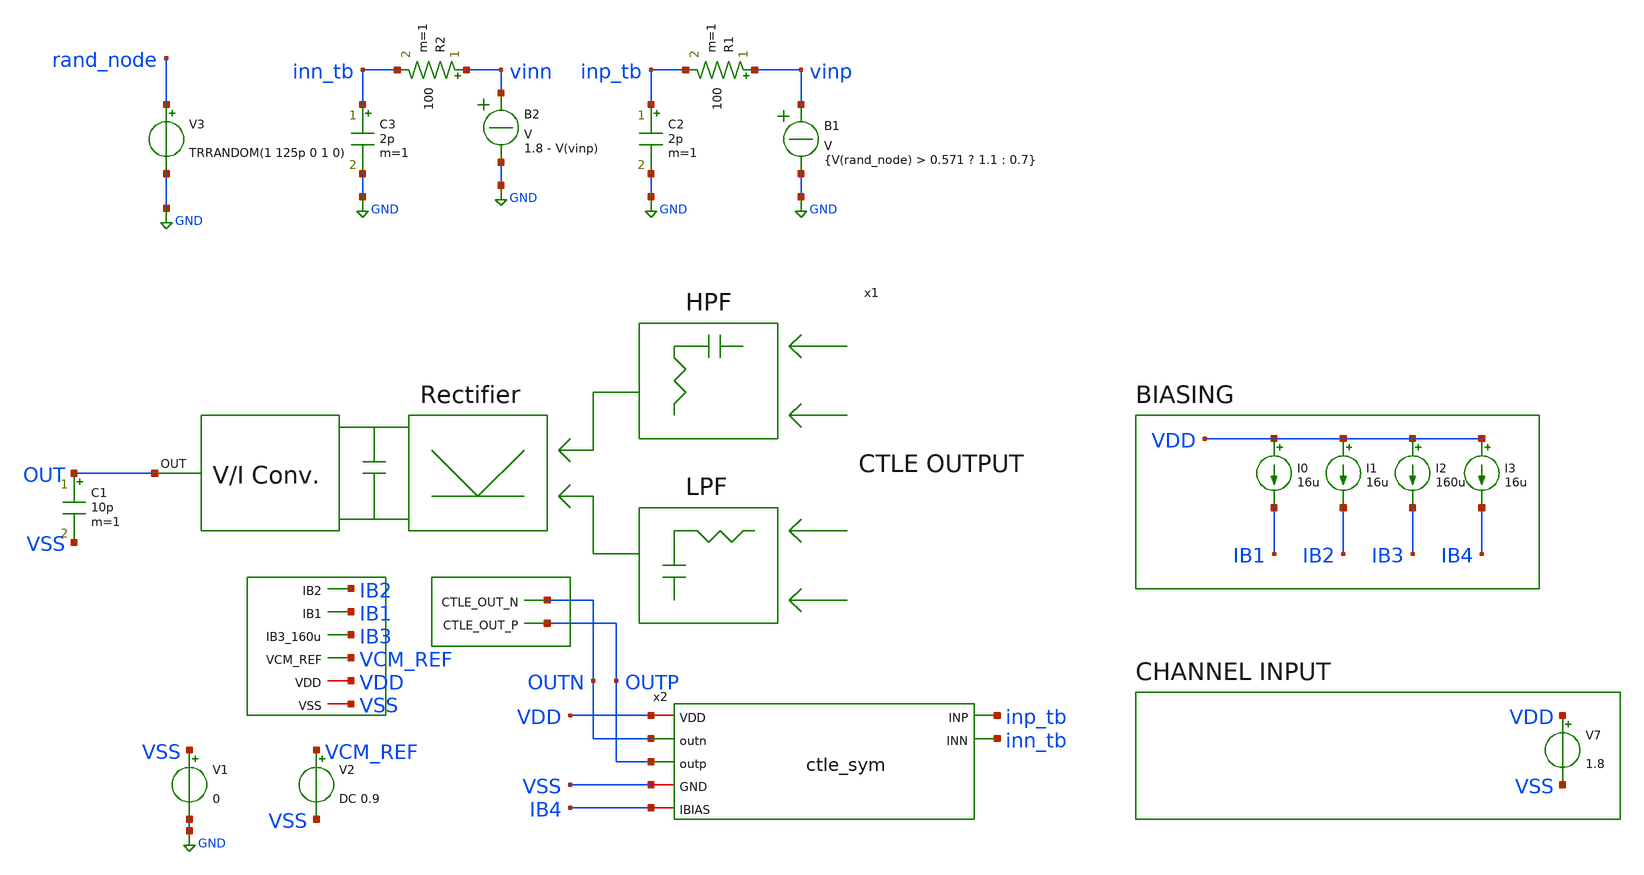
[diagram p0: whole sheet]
** sch_path: pd-converter/tb_adaptation-loop-baseline.sch
**.subckt tb_adaptation-loop-baseline
x1 IB2 VDD OUT IB1 VSS VCM_REF IB3 OUTN OUTP vctrl-generator
x2 VDD OUTN OUTP inp_tb inn_tb VSS IB4 ctle_sym
I0 VDD IB1 16u
I1 VDD IB2 16u
I2 VDD IB3 160u
V7 VDD VSS 1.8
I3 VDD IB4 16u
V1 VSS GND 0
V2 VCM_REF VSS DC 0.9
C1 OUT VSS 10p m=1
R1 vinp inp_tb 100 m=1
C2 inp_tb GND 2p m=1
V3 rand_node GND TRRANDOM(1 125p 0 1 0)
R2 vinn inn_tb 100 m=1
C3 inn_tb GND 2p m=1
B1 vinp GND V = {V(rand_node) > 0.571 ? 1.1 : 0.7}
B2 vinn GND V = 1.8 - V(vinp)
**** begin user architecture code

.lib /foss/pdks/sky130A/libs.tech/ngspice/sky130.lib.spice tt

.control
  tran 1p 500n

  * --- Eye diagram (same as tb_eye) ---
  let period = 250e-12
  let t_mod = time - floor(time / period) * period
  plot v(outp) vs t_mod title Eye - outp
  plot v(outp) v(outn) vs t_mod title Differential Eye

  * --- Adaptation convergence ---
  plot v(OUT) title IBIAS adaptation convergence

  * --- Compare: adaptation vs fixed bias eye quality ---
  * Run twice: once with Xadapt, once with ibias_adapt=ibias_ref fixed
  * and visually compare eye opening

  * --- Measurements ---
  meas tran vout_max  MAX  v(outp)  FROM=50n  TO=100n
  meas tran vout_min  MIN  v(outp)  FROM=50n  TO=100n
  let eye_height_single = vout_max - vout_min
  print eye_height_single

  meas tran ibias_final  AVG  v(OUT)  FROM=80n  TO=100n
  print ibias_final

.endc


**** end user architecture code
**.ends

* expanding   symbol:  vctrl-generator.sym # of pins=9
** sym_path: pd-converter/vctrl-generator.sym
** sch_path: pd-converter/vctrl-generator.sch
.subckt vctrl-generator IB2 VDD OUT IB1 VSS VCM_REF IB3_160u CTLE_OUT_N CTLE_OUT_P
*.ipin IB1
*.ipin IB2
*.ipin IB3_160u
*.iopin VDD
*.iopin VSS
*.opin OUT
*.ipin CTLE_OUT_N
*.ipin CTLE_OUT_P
*.ipin VCM_REF
x1 VDD net1 net2 IB3_160u VSS VCM_REF CTLE_OUT_N CTLE_OUT_P filterred_power_detector_sizing
x2 VDD IB2 IB1 OUT net2 net1 VCM_REF VSS voltage-to-i-converter
.ends


* expanding   symbol:  /foss/designs/afe-icdec-teknofest-2026/CTLE/ctle_sym.sym # of pins=7
** sym_path: CTLE/ctle_sym.sym
** sch_path: CTLE/ctle_sym.sch
.subckt ctle_sym VDD outn outp INP INN GND IBIAS
*.opin outp
*.opin outn
*.ipin INN
*.iopin VDD
*.iopin GND
*.iopin IBIAS
*.ipin INP
XM1 outp INP net1 GND sky130_fd_pr__nfet_01v8_lvt L=0.15 W=2 nf=1 ad='int((nf+1)/2) * W/nf * 0.29' as='int((nf+2)/2) * W/nf * 0.29'
+ pd='2*int((nf+1)/2) * (W/nf + 0.29)' ps='2*int((nf+2)/2) * (W/nf + 0.29)' nrd='0.29 / W' nrs='0.29 / W'
+ sa=0 sb=0 sd=0 mult=15 m=15
XM2 outn INN net2 GND sky130_fd_pr__nfet_01v8_lvt L=0.15 W=2 nf=1 ad='int((nf+1)/2) * W/nf * 0.29' as='int((nf+2)/2) * W/nf * 0.29'
+ pd='2*int((nf+1)/2) * (W/nf + 0.29)' ps='2*int((nf+2)/2) * (W/nf + 0.29)' nrd='0.29 / W' nrs='0.29 / W'
+ sa=0 sb=0 sd=0 mult=15 m=15
XM3 net1 IBIAS GND GND sky130_fd_pr__nfet_01v8_lvt L=1 W=2 nf=1 ad='int((nf+1)/2) * W/nf * 0.29' as='int((nf+2)/2) * W/nf * 0.29'
+ pd='2*int((nf+1)/2) * (W/nf + 0.29)' ps='2*int((nf+2)/2) * (W/nf + 0.29)' nrd='0.29 / W' nrs='0.29 / W'
+ sa=0 sb=0 sd=0 mult=24 m=24
XM4 net2 IBIAS GND GND sky130_fd_pr__nfet_01v8_lvt L=1 W=2 nf=1 ad='int((nf+1)/2) * W/nf * 0.29' as='int((nf+2)/2) * W/nf * 0.29'
+ pd='2*int((nf+1)/2) * (W/nf + 0.29)' ps='2*int((nf+2)/2) * (W/nf + 0.29)' nrd='0.29 / W' nrs='0.29 / W'
+ sa=0 sb=0 sd=0 mult=24 m=24
XM5 IBIAS IBIAS GND GND sky130_fd_pr__nfet_01v8_lvt L=1 W=2 nf=1 ad='int((nf+1)/2) * W/nf * 0.29' as='int((nf+2)/2) * W/nf * 0.29'
+ pd='2*int((nf+1)/2) * (W/nf + 0.29)' ps='2*int((nf+2)/2) * (W/nf + 0.29)' nrd='0.29 / W' nrs='0.29 / W'
+ sa=0 sb=0 sd=0 mult=1 m=1
RD1 VDD outp 280 m=1
RD2 VDD outn 280 m=1
CS net1 net2 134f m=1
RS net1 net2 1400 m=1
C1 outp GND 20f m=1
C2 outn GND 20f m=1
.ends


* expanding   symbol:
*+  /foss/designs/afe-icdec-teknofest-2026/CTLE/filterred_power_detector_sizing.sym # of pins=8
** sym_path: CTLE/filterred_power_detector_sizing.sym
** sch_path: CTLE/filterred_power_detector_sizing.sch
.subckt filterred_power_detector_sizing vdd voutp voutn ibias vss vcmref vinn vinp
*.ipin vinp
*.ipin vinn
*.opin voutp
*.opin voutn
*.ipin ibias
*.iopin vss
*.iopin vdd
*.ipin vcmref
XM1 voutp Vhf_pos net1 vss sky130_fd_pr__nfet_01v8 L=0.45 W=1.23 nf=1 ad='int((nf+1)/2) * W/nf * 0.29'
+ as='int((nf+2)/2) * W/nf * 0.29' pd='2*int((nf+1)/2) * (W/nf + 0.29)' ps='2*int((nf+2)/2) * (W/nf + 0.29)'
+ nrd='0.29 / W' nrs='0.29 / W' sa=0 sb=0 sd=0 mult=1 m=1
XM2 voutp Vhf_neg net1 vss sky130_fd_pr__nfet_01v8 L=0.45 W=1.23 nf=1 ad='int((nf+1)/2) * W/nf * 0.29'
+ as='int((nf+2)/2) * W/nf * 0.29' pd='2*int((nf+1)/2) * (W/nf + 0.29)' ps='2*int((nf+2)/2) * (W/nf + 0.29)'
+ nrd='0.29 / W' nrs='0.29 / W' sa=0 sb=0 sd=0 mult=1 m=1
XM3 voutn Vlf_pos net1 vss sky130_fd_pr__nfet_01v8 L=0.75 W=1.23 nf=1 ad='int((nf+1)/2) * W/nf * 0.29'
+ as='int((nf+2)/2) * W/nf * 0.29' pd='2*int((nf+1)/2) * (W/nf + 0.29)' ps='2*int((nf+2)/2) * (W/nf + 0.29)'
+ nrd='0.29 / W' nrs='0.29 / W' sa=0 sb=0 sd=0 mult=1 m=1
XM4 voutn Vlf_neg net1 vss sky130_fd_pr__nfet_01v8 L=0.45 W=1.23 nf=1 ad='int((nf+1)/2) * W/nf * 0.29'
+ as='int((nf+2)/2) * W/nf * 0.29' pd='2*int((nf+1)/2) * (W/nf + 0.29)' ps='2*int((nf+2)/2) * (W/nf + 0.29)'
+ nrd='0.29 / W' nrs='0.29 / W' sa=0 sb=0 sd=0 mult=1 m=1
XC7 Vhf_neg vinn sky130_fd_pr__cap_mim_m3_1 W=5.7921 L=5.7921 MF=1 m=1
XC3 Vhf_pos vinp sky130_fd_pr__cap_mim_m3_1 W=5.7921 L=5.7921 MF=1 m=1
XR9 Vhf_neg net2 vss sky130_fd_pr__res_high_po_5p73 L=69.65 mult=4 m=4
XR3 net2 Vhf_pos vss sky130_fd_pr__res_high_po_5p73 L=69.65 mult=4 m=4
XR4 vcmref vinn vss sky130_fd_pr__res_high_po_5p73 L=708 mult=4 m=4
XR5 vinp vcmref vss sky130_fd_pr__res_high_po_5p73 L=708 mult=4 m=4
XC4 net2 vss sky130_fd_pr__cap_mim_m3_1 W=0.4208 L=0.4208 MF=1 m=1
XR6 Vlf_pos vinp vss sky130_fd_pr__res_high_po_5p73 L=69.65 mult=4 m=4
XR7 vinn Vlf_neg vss sky130_fd_pr__res_high_po_5p73 L=69.65 mult=4 m=4
XC2 Vlf_pos vss sky130_fd_pr__cap_mim_m3_1 W=5.7921 L=5.7921 MF=1 m=1
XC5 vss Vlf_neg sky130_fd_pr__cap_mim_m3_1 W=5.7921 L=5.7921 MF=1 m=1
XC6 voutp voutn sky130_fd_pr__cap_mim_m3_1 W=0.2019 L=0.2019 MF=1 m=1
XR8 voutp vdd vss sky130_fd_pr__res_high_po_5p73 L=796.338 mult=4 m=4
XR1 voutn vdd vss sky130_fd_pr__res_high_po_5p73 L=796.338 mult=4 m=4
XM5 net1 ibias vss vss sky130_fd_pr__nfet_01v8 L=0.45 W=4.92 nf=1 ad='int((nf+1)/2) * W/nf * 0.29' as='int((nf+2)/2) * W/nf * 0.29'
+ pd='2*int((nf+1)/2) * (W/nf + 0.29)' ps='2*int((nf+2)/2) * (W/nf + 0.29)' nrd='0.29 / W' nrs='0.29 / W'
+ sa=0 sb=0 sd=0 mult=1 m=1
XM6 ibias ibias vss vss sky130_fd_pr__nfet_01v8 L=0.45 W=0.45 nf=1 ad='int((nf+1)/2) * W/nf * 0.29' as='int((nf+2)/2) * W/nf * 0.29'
+ pd='2*int((nf+1)/2) * (W/nf + 0.29)' ps='2*int((nf+2)/2) * (W/nf + 0.29)' nrd='0.29 / W' nrs='0.29 / W'
+ sa=0 sb=0 sd=0 mult=1 m=1
.ends


* expanding   symbol:  /foss/designs/afe-icdec-teknofest-2026/CTLE/voltage-to-i-converter.sym # of
*+ pins=8
** sym_path: CTLE/voltage-to-i-converter.sym
** sch_path: CTLE/voltage-to-i-converter.sch
.subckt voltage-to-i-converter VDD IB2_16u IB1_16u OUT DOWN UP vcmref VSS
*.iopin VDD
*.iopin VSS
*.opin OUT
*.ipin IB2_16u
*.ipin UP
*.ipin DOWN
*.ipin IB1_16u
*.ipin vcmref
XM1 net3 net3 VDD VDD sky130_fd_pr__pfet_01v8 L=0.6 W=75 nf=1 ad='int((nf+1)/2) * W/nf * 0.29' as='int((nf+2)/2) * W/nf * 0.29'
+ pd='2*int((nf+1)/2) * (W/nf + 0.29)' ps='2*int((nf+2)/2) * (W/nf + 0.29)' nrd='0.29 / W' nrs='0.29 / W'
+ sa=0 sb=0 sd=0 mult=1 m=1
XM2 net5 net5 VDD VDD sky130_fd_pr__pfet_01v8 L=0.6 W=75 nf=1 ad='int((nf+1)/2) * W/nf * 0.29' as='int((nf+2)/2) * W/nf * 0.29'
+ pd='2*int((nf+1)/2) * (W/nf + 0.29)' ps='2*int((nf+2)/2) * (W/nf + 0.29)' nrd='0.29 / W' nrs='0.29 / W'
+ sa=0 sb=0 sd=0 mult=1 m=1
XM5 net1 IB1_16u VSS VSS sky130_fd_pr__nfet_01v8 L=1.5 W=25 nf=1 ad='int((nf+1)/2) * W/nf * 0.29' as='int((nf+2)/2) * W/nf * 0.29'
+ pd='2*int((nf+1)/2) * (W/nf + 0.29)' ps='2*int((nf+2)/2) * (W/nf + 0.29)' nrd='0.29 / W' nrs='0.29 / W'
+ sa=0 sb=0 sd=0 mult=1 m=1
XM6 IB1_16u IB1_16u VSS VSS sky130_fd_pr__nfet_01v8 L=1.5 W=25 nf=1 ad='int((nf+1)/2) * W/nf * 0.29'
+ as='int((nf+2)/2) * W/nf * 0.29' pd='2*int((nf+1)/2) * (W/nf + 0.29)' ps='2*int((nf+2)/2) * (W/nf + 0.29)'
+ nrd='0.29 / W' nrs='0.29 / W' sa=0 sb=0 sd=0 mult=1 m=1
XM7 net4 net4 VDD VDD sky130_fd_pr__pfet_01v8 L=0.6 W=75 nf=1 ad='int((nf+1)/2) * W/nf * 0.29' as='int((nf+2)/2) * W/nf * 0.29'
+ pd='2*int((nf+1)/2) * (W/nf + 0.29)' ps='2*int((nf+2)/2) * (W/nf + 0.29)' nrd='0.29 / W' nrs='0.29 / W'
+ sa=0 sb=0 sd=0 mult=1 m=1
XM8 net6 net6 VDD VDD sky130_fd_pr__pfet_01v8 L=0.6 W=75 nf=1 ad='int((nf+1)/2) * W/nf * 0.29' as='int((nf+2)/2) * W/nf * 0.29'
+ pd='2*int((nf+1)/2) * (W/nf + 0.29)' ps='2*int((nf+2)/2) * (W/nf + 0.29)' nrd='0.29 / W' nrs='0.29 / W'
+ sa=0 sb=0 sd=0 mult=1 m=1
XM11 net2 IB2_16u VSS VSS sky130_fd_pr__nfet_01v8 L=1.5 W=25 nf=1 ad='int((nf+1)/2) * W/nf * 0.29' as='int((nf+2)/2) * W/nf * 0.29'
+ pd='2*int((nf+1)/2) * (W/nf + 0.29)' ps='2*int((nf+2)/2) * (W/nf + 0.29)' nrd='0.29 / W' nrs='0.29 / W'
+ sa=0 sb=0 sd=0 mult=1 m=1
XM12 IB2_16u IB2_16u VSS VSS sky130_fd_pr__nfet_01v8 L=1.5 W=25 nf=1 ad='int((nf+1)/2) * W/nf * 0.29'
+ as='int((nf+2)/2) * W/nf * 0.29' pd='2*int((nf+1)/2) * (W/nf + 0.29)' ps='2*int((nf+2)/2) * (W/nf + 0.29)'
+ nrd='0.29 / W' nrs='0.29 / W' sa=0 sb=0 sd=0 mult=1 m=1
XM13 OUT net6 VDD VDD sky130_fd_pr__pfet_01v8 L=0.6 W=75 nf=1 ad='int((nf+1)/2) * W/nf * 0.29' as='int((nf+2)/2) * W/nf * 0.29'
+ pd='2*int((nf+1)/2) * (W/nf + 0.29)' ps='2*int((nf+2)/2) * (W/nf + 0.29)' nrd='0.29 / W' nrs='0.29 / W'
+ sa=0 sb=0 sd=0 mult=1 m=1
XM14 net7 net5 VDD VDD sky130_fd_pr__pfet_01v8 L=0.6 W=75 nf=1 ad='int((nf+1)/2) * W/nf * 0.29' as='int((nf+2)/2) * W/nf * 0.29'
+ pd='2*int((nf+1)/2) * (W/nf + 0.29)' ps='2*int((nf+2)/2) * (W/nf + 0.29)' nrd='0.29 / W' nrs='0.29 / W'
+ sa=0 sb=0 sd=0 mult=1 m=1
XM15 net7 net7 VSS VSS sky130_fd_pr__nfet_01v8 L=1.5 W=25 nf=1 ad='int((nf+1)/2) * W/nf * 0.29' as='int((nf+2)/2) * W/nf * 0.29'
+ pd='2*int((nf+1)/2) * (W/nf + 0.29)' ps='2*int((nf+2)/2) * (W/nf + 0.29)' nrd='0.29 / W' nrs='0.29 / W'
+ sa=0 sb=0 sd=0 mult=1 m=1
XM16 OUT net7 VSS VSS sky130_fd_pr__nfet_01v8 L=1.5 W=25 nf=1 ad='int((nf+1)/2) * W/nf * 0.29' as='int((nf+2)/2) * W/nf * 0.29'
+ pd='2*int((nf+1)/2) * (W/nf + 0.29)' ps='2*int((nf+2)/2) * (W/nf + 0.29)' nrd='0.29 / W' nrs='0.29 / W'
+ sa=0 sb=0 sd=0 mult=1 m=1
XR1 DOWN vcmref VSS sky130_fd_pr__res_high_po_0p35 L=50 mult=1 m=1
XR2 vcmref UP VSS sky130_fd_pr__res_high_po_0p35 L=50 mult=1 m=1
XC1 OUT VSS sky130_fd_pr__cap_mim_m3_1 W=30 L=30 MF=4 m=4
XM3 net5 DOWN net1 VSS sky130_fd_pr__nfet_01v8 L=0.5 W=25 nf=1 ad='int((nf+1)/2) * W/nf * 0.29' as='int((nf+2)/2) * W/nf * 0.29'
+ pd='2*int((nf+1)/2) * (W/nf + 0.29)' ps='2*int((nf+2)/2) * (W/nf + 0.29)' nrd='0.29 / W' nrs='0.29 / W'
+ sa=0 sb=0 sd=0 mult=1 m=1
XM4 net3 vcmref net1 VSS sky130_fd_pr__nfet_01v8 L=0.5 W=25 nf=1 ad='int((nf+1)/2) * W/nf * 0.29' as='int((nf+2)/2) * W/nf * 0.29'
+ pd='2*int((nf+1)/2) * (W/nf + 0.29)' ps='2*int((nf+2)/2) * (W/nf + 0.29)' nrd='0.29 / W' nrs='0.29 / W'
+ sa=0 sb=0 sd=0 mult=1 m=1
XM9 net4 vcmref net2 VSS sky130_fd_pr__nfet_01v8 L=0.5 W=25 nf=1 ad='int((nf+1)/2) * W/nf * 0.29' as='int((nf+2)/2) * W/nf * 0.29'
+ pd='2*int((nf+1)/2) * (W/nf + 0.29)' ps='2*int((nf+2)/2) * (W/nf + 0.29)' nrd='0.29 / W' nrs='0.29 / W'
+ sa=0 sb=0 sd=0 mult=1 m=1
XM10 net6 UP net2 VSS sky130_fd_pr__nfet_01v8 L=0.5 W=25 nf=1 ad='int((nf+1)/2) * W/nf * 0.29' as='int((nf+2)/2) * W/nf * 0.29'
+ pd='2*int((nf+1)/2) * (W/nf + 0.29)' ps='2*int((nf+2)/2) * (W/nf + 0.29)' nrd='0.29 / W' nrs='0.29 / W'
+ sa=0 sb=0 sd=0 mult=1 m=1
.ends

.GLOBAL GND
.end
